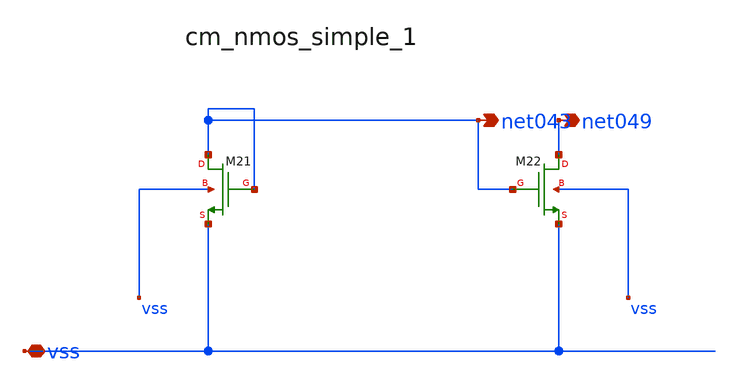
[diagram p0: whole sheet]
** sch_path: analog-db/raw/amp_003_fan_smc/hier/blocks/cm_nmos_simple_1.sch
**.subckt cm_nmos_simple_1 vss net043 net049
*.iopin vss
*.opin net043
*.opin net049
XM21 net043 net043 vss vss sg13_lv_nmos w=x_dut_xm21_w l=x_dut_xm21_l ng=1 m=x_dut_xm21_m
XM22 net049 net043 vss vss sg13_lv_nmos w=x_dut_xm22_w l=x_dut_xm22_l ng=1 m=x_dut_xm22_m
**.ends
.end
